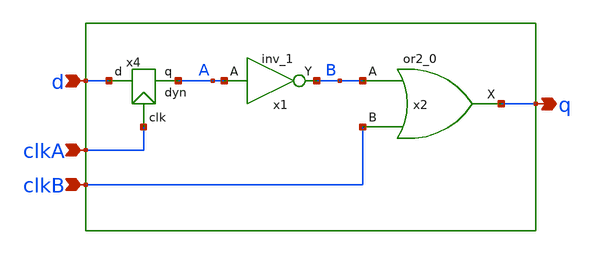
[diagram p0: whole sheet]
** sch_path: src/xe/test_cases/dyn_or.sch
**.subckt dyn_or d clkA q clkB
*.ipin d
*.ipin clkA
*.opin q
*.ipin clkB
x1 A vss vss vcc vcc B sky130_fd_sc_hd__inv_1
x4 clkA A d dyn
x2 B clkB vss vss vcc vcc q sky130_fd_sc_hd__or2_0
**.ends

* expanding   symbol:  yxt/dyn.sym # of pins=3
** sym_path: src/xe/test_cases/dyn.sym
** sch_path: src/xe/test_cases/dyn.sch
.subckt dyn clk q d
*.ipin clk
*.opin q
*.ipin d
x1 net1 vss vss vcc vcc q sky130_fd_sc_hd__inv_1
XM1 net1 d net2 vss sky130_fd_pr__nfet_01v8 L=0.15 W=1 nf=1 ad='int((nf+1)/2) * W/nf * 0.29' as='int((nf+2)/2) * W/nf * 0.29'
+ pd='2*int((nf+1)/2) * (W/nf + 0.29)' ps='2*int((nf+2)/2) * (W/nf + 0.29)' nrd='0.29 / W' nrs='0.29 / W'
+ sa=0 sb=0 sd=0 mult=1 m=1
XM2 net1 q vcc vcc sky130_fd_pr__pfet_01v8 L=0.15 W=1 nf=1 ad='int((nf+1)/2) * W/nf * 0.29' as='int((nf+2)/2) * W/nf * 0.29'
+ pd='2*int((nf+1)/2) * (W/nf + 0.29)' ps='2*int((nf+2)/2) * (W/nf + 0.29)' nrd='0.29 / W' nrs='0.29 / W'
+ sa=0 sb=0 sd=0 mult=1 m=1
XM3 net1 clk vcc vcc sky130_fd_pr__pfet_01v8 L=0.15 W=1 nf=1 ad='int((nf+1)/2) * W/nf * 0.29' as='int((nf+2)/2) * W/nf * 0.29'
+ pd='2*int((nf+1)/2) * (W/nf + 0.29)' ps='2*int((nf+2)/2) * (W/nf + 0.29)' nrd='0.29 / W' nrs='0.29 / W'
+ sa=0 sb=0 sd=0 mult=1 m=1
XM4 net2 clk vss vss sky130_fd_pr__nfet_01v8 L=0.15 W=1 nf=1 ad='int((nf+1)/2) * W/nf * 0.29' as='int((nf+2)/2) * W/nf * 0.29'
+ pd='2*int((nf+1)/2) * (W/nf + 0.29)' ps='2*int((nf+2)/2) * (W/nf + 0.29)' nrd='0.29 / W' nrs='0.29 / W'
+ sa=0 sb=0 sd=0 mult=1 m=1
.ends

.end
